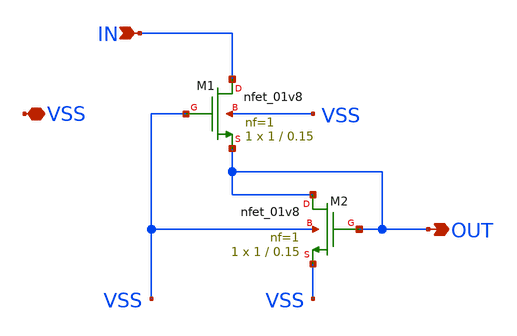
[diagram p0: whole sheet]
** sch_path: xschem/vref.sch
**.subckt vref VSS IN OUT
*.iopin VSS
*.ipin IN
*.opin OUT
XM1 IN VSS OUT VSS sky130_fd_pr__nfet_01v8 L=0.15 W=1 nf=1 ad='int((nf+1)/2) * W/nf * 0.29' as='int((nf+2)/2) * W/nf * 0.29'
+ pd='2*int((nf+1)/2) * (W/nf + 0.29)' ps='2*int((nf+2)/2) * (W/nf + 0.29)' nrd='0.29 / W' nrs='0.29 / W'
+ sa=0 sb=0 sd=0 mult=1 m=1
XM2 OUT OUT VSS VSS sky130_fd_pr__nfet_01v8 L=0.15 W=1 nf=1 ad='int((nf+1)/2) * W/nf * 0.29' as='int((nf+2)/2) * W/nf * 0.29'
+ pd='2*int((nf+1)/2) * (W/nf + 0.29)' ps='2*int((nf+2)/2) * (W/nf + 0.29)' nrd='0.29 / W' nrs='0.29 / W'
+ sa=0 sb=0 sd=0 mult=1 m=1
**.ends
.end
